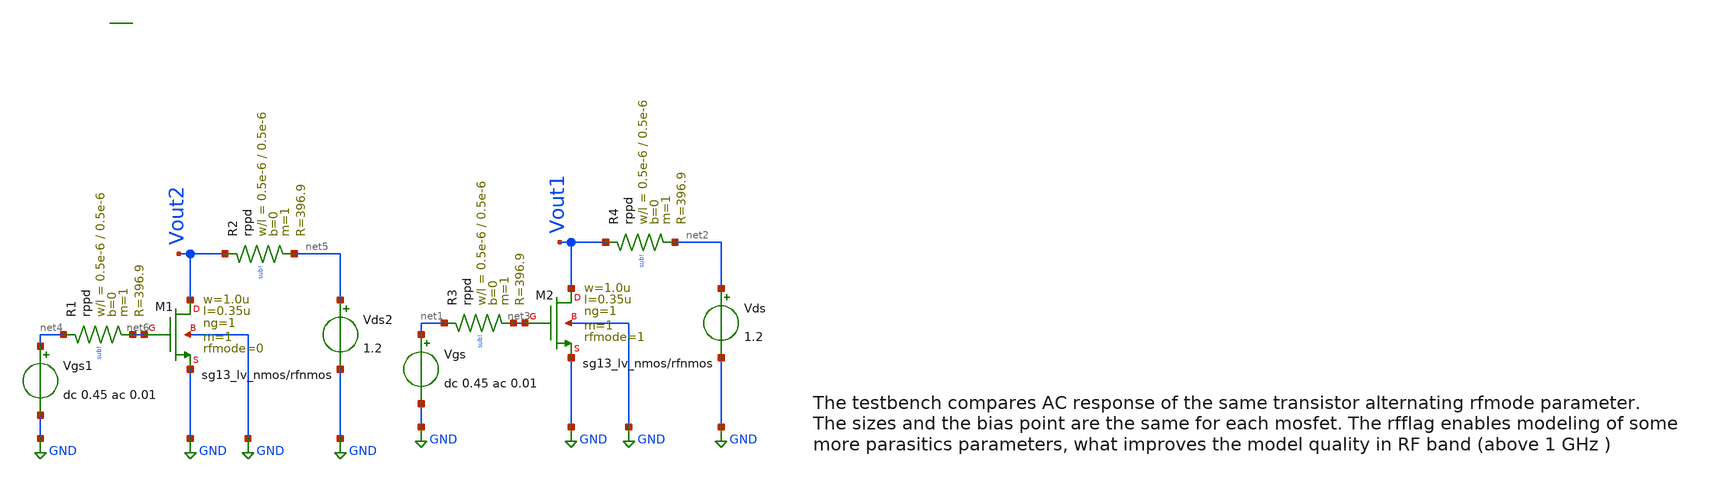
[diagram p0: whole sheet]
** sch_path: ihp-sg13g2/xschem_libs/sg13g2_tests_ase/ac_lv_nmosrf/schematic/ac_lv_nmosrf.sch
* Copyright 2023 IHP PDK Authors
**.subckt ac_lv_nmosrf
Vgs net1 GND dc 0.45 ac 0.01
Vds net2 GND 1.2
Vgs1 net4 GND dc 0.45 ac 0.01
Vds2 net5 GND 1.2
XR1 net4 net6 sub! rppd w=0.5e-6 l=0.5e-6 m=1 b=0 mm_ok=1
XR2 Vout2 net5 sub! rppd w=0.5e-6 l=0.5e-6 m=1 b=0 mm_ok=1
XR3 net1 net3 sub! rppd w=0.5e-6 l=0.5e-6 m=1 b=0 mm_ok=1
XR4 Vout1 net2 sub! rppd w=0.5e-6 l=0.5e-6 m=1 b=0 mm_ok=1
XM1 Vout2 net6 GND GND sg13_lv_nmos w=1.0u l=0.35u ng=1 m=1 rfmode=0 mm_ok=1
XM2 Vout1 net3 GND GND sg13_lv_nmos w=1.0u l=0.35u ng=1 m=1 rfmode=1 mm_ok=1
**.ends
.GLOBAL GND
.end
